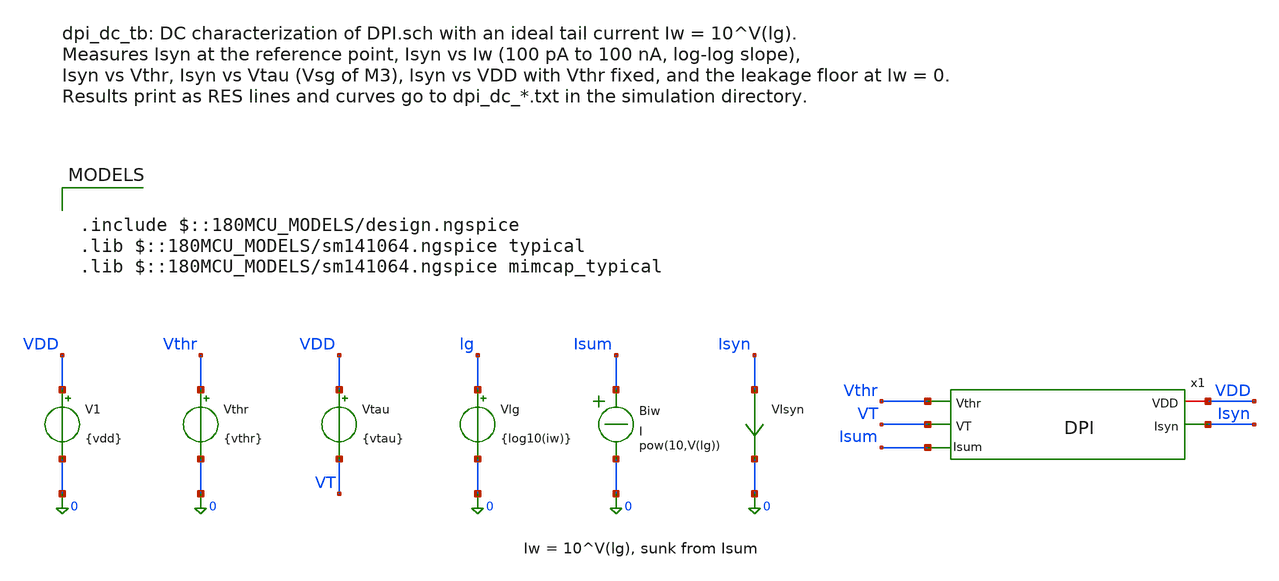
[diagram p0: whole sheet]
** sch_path: analog/testbenches/dpi/dpi_dc_tb.sch
**.subckt dpi_dc_tb
V1 VDD 0 {vdd}
Vthr Vthr 0 {vthr}
Vtau VDD VT {vtau}
Vlg lg 0 {log10(iw)}
Biw Isum 0 I = pow(10,V(lg))
VIsyn Isyn 0 0
.save i(visyn)
x1 VDD Vthr Isyn Isum VT DPI
**** begin user architecture code


* Reference operating point (see analog/testbenches/README.md)
.param vdd=3.3 vthr=2.9 vtau=0.40 iw=5n
.csparam iw_c={iw}
.csparam vthr_c={vthr}
.csparam vtau_c={vtau}
.csparam vdd_c={vdd}
.control
  save all
  set wr_singlescale
  set wr_vecnames
  let lg_nom = log10(iw_c)
  let lg_lo = lg_nom - 1
  let lg_hi = lg_nom + 1

  * 0) Operating point at the reference bias
  op
  let isyn_op = i(VIsyn)
  let gain_op = isyn_op/iw_c
  let ivdd_op = -i(V1)
  let vsum_op = v(Isum)
  let vsyn_op = v(x1.net1)
  echo RES isyn_op=$&isyn_op
  echo RES gain_op=$&gain_op
  echo RES ivdd_op=$&ivdd_op
  echo RES vsum_op=$&vsum_op
  echo RES vsyn_op=$&vsyn_op

  * 1) Isyn vs Iw, 100 pA to 100 nA
  dc Vlg -10 -7 0.02
  let iw = 10^v(lg)
  let isyn = i(VIsyn)
  meas dc isyn_lo find isyn at=$&lg_lo
  meas dc isyn_hi find isyn at=$&lg_hi
  let slope_iw = log10(isyn_hi/isyn_lo)/2
  echo RES slope_iw=$&slope_iw
  wrdata dpi_dc_iw.txt iw isyn v(Isum) v(x1.net1)
  if $?batchmode = 0
    plot isyn vs iw loglog title 'Isyn vs Iw' xlabel 'Iw (A)' ylabel 'Isyn (A)'
  end

  * 2) Isyn vs Vthr
  dc Vthr 2.6 3.2 2m
  let isyn = i(VIsyn)
  let va = vthr_c - 0.05
  let vb = vthr_c + 0.05
  meas dc i_a find isyn at=$&va
  meas dc i_b find isyn at=$&vb
  let mvdec_vthr = 100/log10(i_a/i_b)
  echo RES mvdec_vthr=$&mvdec_vthr
  wrdata dpi_dc_vthr.txt isyn
  if $?batchmode = 0
    plot ylog isyn title 'Isyn vs Vthr' xlabel 'Vthr (V)' ylabel 'Isyn (A)'
  end

  * 3) Isyn vs Vtau (Vsg of the tau pFET M3)
  dc Vtau 0.30 0.50 1m
  let isyn = i(VIsyn)
  let va = vtau_c - 0.05
  let vb = vtau_c + 0.05
  meas dc i_a find isyn at=$&va
  meas dc i_b find isyn at=$&vb
  let mvdec_vtau = 100/log10(i_a/i_b)
  echo RES mvdec_vtau=$&mvdec_vtau
  wrdata dpi_dc_vtau.txt isyn
  if $?batchmode = 0
    plot ylog isyn title 'Isyn vs Vtau' xlabel 'Vtau = Vsg(M3) (V)' ylabel 'Isyn (A)'
  end

  * 4) Isyn vs VDD with Vthr fixed (Vtau follows VDD)
  dc V1 3.0 3.6 5m
  let isyn = i(VIsyn)
  let va = vdd_c - 0.1
  let vb = vdd_c + 0.1
  meas dc i_a find isyn at=$&va
  meas dc i_b find isyn at=$&vb
  let mvdec_vdd = 200/log10(i_b/i_a)
  echo RES mvdec_vdd=$&mvdec_vdd
  wrdata dpi_dc_vdd.txt isyn
  if $?batchmode = 0
    plot ylog isyn title 'Isyn vs VDD (Vthr fixed)' xlabel 'VDD (V)' ylabel 'Isyn (A)'
  end

  * 5) Leakage floor with no input current
  alter Vlg dc=-20
  op
  let i_leak = i(VIsyn)
  echo RES i_leak=$&i_leak
.endc



.include $::180MCU_MODELS/design.ngspice
.lib $::180MCU_MODELS/sm141064.ngspice typical
.lib $::180MCU_MODELS/sm141064.ngspice mimcap_typical

**** end user architecture code
**.ends

* expanding   symbol:  DPI.sym # of pins=5
** sym_path: analog/neuron/DPI.sym
** sch_path: analog/neuron/DPI.sch
.subckt DPI VDD Vthr Isyn Isum VT
*.ipin Vthr
*.iopin VDD
*.opin Isyn
*.opin Isum
*.ipin VT
XM1 VDD Vthr Isum Isum nfet_03v3 L=0.28u W=0.22u nf=1 ad='int((nf+1)/2) * W/nf * 0.18u' as='int((nf+2)/2) * W/nf * 0.18u'
+ pd='2*int((nf+1)/2) * (W/nf + 0.18u)' ps='2*int((nf+2)/2) * (W/nf + 0.18u)' nrd='0.18u / W' nrs='0.18u / W'
+ sa=0 sb=0 sd=0 m=1
XM2 net1 net1 Isum Isum nfet_03v3 L=0.28u W=0.22u nf=1 ad='int((nf+1)/2) * W/nf * 0.18u' as='int((nf+2)/2) * W/nf * 0.18u'
+ pd='2*int((nf+1)/2) * (W/nf + 0.18u)' ps='2*int((nf+2)/2) * (W/nf + 0.18u)' nrd='0.18u / W' nrs='0.18u / W'
+ sa=0 sb=0 sd=0 m=1
XM3 net1 VT VDD VDD pfet_03v3 L=0.28u W=0.22u nf=1 ad='int((nf+1)/2) * W/nf * 0.18u' as='int((nf+2)/2) * W/nf * 0.18u'
+ pd='2*int((nf+1)/2) * (W/nf + 0.18u)' ps='2*int((nf+2)/2) * (W/nf + 0.18u)' nrd='0.18u / W' nrs='0.18u / W'
+ sa=0 sb=0 sd=0 m=1
XM4 Isyn net1 VDD VDD pfet_03v3 L=0.28u W=0.22u nf=1 ad='int((nf+1)/2) * W/nf * 0.18u' as='int((nf+2)/2) * W/nf * 0.18u'
+ pd='2*int((nf+1)/2) * (W/nf + 0.18u)' ps='2*int((nf+2)/2) * (W/nf + 0.18u)' nrd='0.18u / W' nrs='0.18u / W'
+ sa=0 sb=0 sd=0 m=1
C4 VDD net1 1p m=1
.ends

.end
